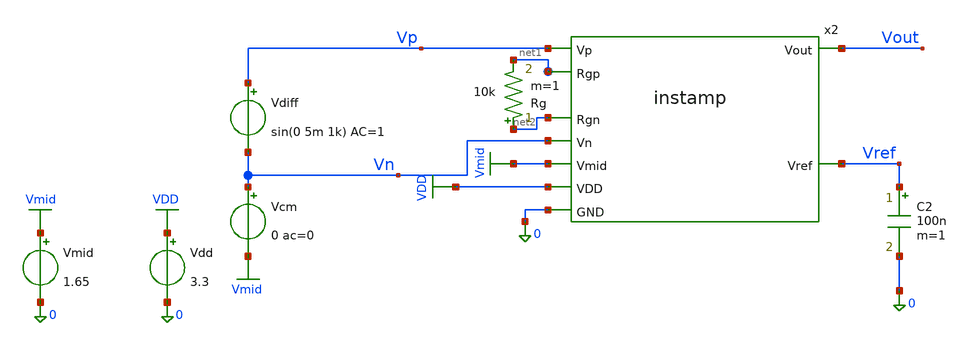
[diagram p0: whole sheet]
** sch_path: xschem/instamp_tb.sch
* Copyright 2021 Stefan Frederik Schippers
* Licensed under the Apache License, Version 2.0 (the "License");
* you may not use this file except in compliance with the License.
* You may obtain a copy of the License at
* https://www.apache.org/licenses/LICENSE-2.0
* Unless required by applicable law or agreed to in writing, software
* distributed under the License is distributed on an "AS IS" BASIS,
* WITHOUT WARRANTIES OR CONDITIONS OF ANY KIND, either express or implied.
* See the License for the specific language governing permissions and
* limitations under the License.
**.subckt instamp_tb
Vdd VDD 0 3.3
Vdiff Vp Vn sin(0 5m 1k) AC=1
Vmid Vmid 0 1.65
Vcm Vn Vmid 0 ac=0
x2 Vn net2 Vp net1 Vmid Vout Vref VDD 0 instamp
C2 Vref 0 100n m=1
Rg net2 net1 10k m=1
**** begin user architecture code

** opencircuitdesign pdks install
.lib $::SKYWATER_MODELS/sky130.lib.spice tt



.option wnflag=1
.option savecurrents
.option rshunt=1e12
.include ../netlist/rcx/instamp.spice
.save all
.control
op
write instamp_tb.raw
set appendwrite
set gnuplot_terminal=png/quit

* write instamp_tb.raw
if 0
* differential gain tran
  destroy all
  foreach val 10k 5k 1k
    alter Rg = $val
    tran 10u 3m 1m
  end
  let Rg10k = tran1.v(vout)
  let Rg5k = tran2.v(vout)
  let Rg1k = tran3.v(vout)
  gnuplot tran Rg10k Rg5k Rg1k
*+ title 'Differential gain'  xlabel 'Time' ylabel 'Volts'
endif

* run ac on schematic as drawn
if 1
  destroy all
* differential gain ac
  ac dec 100 1 1Meg
  plot db(v(vout))
endif

* run ac cmrr and psrr sweeps
if 0
  destroy all
* differential gain ac
  alter vdiff ac=1
  alter vcm ac=0
  alter vdd ac=0
  foreach val 10k 5k 1k
    alter Rg = $val
    ac dec 100 1 1Meg
  end
  alter vdiff ac=0
  alter vcm ac=1
  alter vdd ac=0
  foreach val 10k 5k 1k
    alter Rg = $val
    ac dec 100 1 1Meg
  end
  alter vdiff ac=0
  alter vcm ac=0
  alter vdd ac=1
  foreach val 10k 5k 1k
    alter Rg = $val
    ac dec 100 1 1Meg
  end
  alter vdiff ac=0
  alter vcm ac=0
  alter vdd ac=0
  alter vmid ac=1
  foreach val 10k 5k 1k
    alter Rg = $val
    ac dec 100 1 1Meg
  end
  let Rg10k = db(ac1.v(vout))
  let Rg5k = db(ac2.v(vout))
  let Rg1k = db(ac3.v(vout))
  let Rg10k_cm = Rg10k-db(ac4.v(vout))
  let Rg5k_cm = Rg5k-db(ac5.v(vout))
  let Rg1k_cm = Rg1k-db(ac6.v(vout))
  let Rg10k_psh = Rg10k-db(ac7.v(vout))
  let Rg5k_psh = Rg5k-db(ac8.v(vout))
  let Rg1k_psh = Rg1k-db(ac9.v(vout))
  let Rg10k_vmid = Rg10k-db(ac10.v(vout))
  let Rg5k_vmid = Rg5k-db(ac11.v(vout))
  let Rg1k_vmid = Rg1k-db(ac12.v(vout))

  gnuplot ac Rg10k Rg5k Rg1k  title 'Differential gain'  xlabel 'Freq' ylabel 'Gain dB'
  gnuplot cmrr Rg10k_cm Rg5k_cm Rg1k_cm  title 'CMRR'  xlabel 'Freq' ylabel 'Gain dB'
  gnuplot psrr Rg10k_psh Rg5k_psh Rg1k_psh  title 'PSRR'  xlabel 'Freq' ylabel 'Gain dB'
  gnuplot vmid_rej Rg10k_vmid Rg5k_vmid Rg1k_vmid  title 'Vmid Rejection'  xlabel 'Freq' ylabel 'Gain dB'

endif

if 0
* common mode gain
  alter vdiff ac=0
  alter vcm ac=1
  foreach val 90k 5k 1k
    alter Rg = $val
    ac dec 100 1 10Meg
  end

  plot db(ac1.V(Vout)) db(ac2.V(Vout))   db(ac3.V(Vout)) title 'Mag Vout'

* power supply gain
  alter vcm ac=0
  alter vdd ac=1
  foreach val 90k 5k 1k
    alter Rg = $val
    ac dec 100 1 10Meg
  end

  plot db(ac4.V(Vout)) db(ac5.V(Vout))   db(ac6.V(Vout)) title 'Mag Vout'

endif

.endc


**** end user architecture code
**.ends
.GLOBAL VDD
.GLOBAL Vmid
.end
